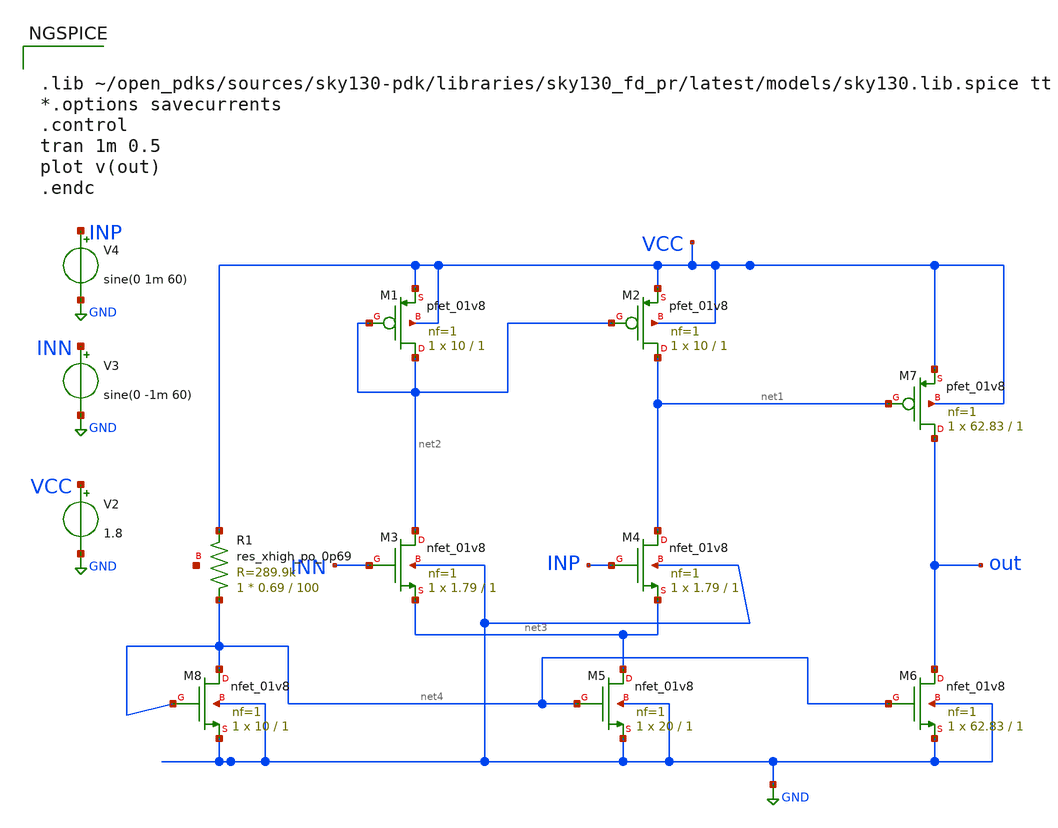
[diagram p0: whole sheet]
** sch_path: Week 4/xschem_180/comp_180.sch
**.subckt comp_180
XM1 net2 net2 VCC VCC sky130_fd_pr__pfet_01v8 L=1 W=10 nf=1 ad='int((nf+1)/2) * W/nf * 0.29' as='int((nf+2)/2) * W/nf * 0.29'
+ pd='2*int((nf+1)/2) * (W/nf + 0.29)' ps='2*int((nf+2)/2) * (W/nf + 0.29)' nrd='0.29 / W' nrs='0.29 / W'
+ sa=0 sb=0 sd=0 mult=1 m=1
XM2 net1 net2 VCC VCC sky130_fd_pr__pfet_01v8 L=1 W=10 nf=1 ad='int((nf+1)/2) * W/nf * 0.29' as='int((nf+2)/2) * W/nf * 0.29'
+ pd='2*int((nf+1)/2) * (W/nf + 0.29)' ps='2*int((nf+2)/2) * (W/nf + 0.29)' nrd='0.29 / W' nrs='0.29 / W'
+ sa=0 sb=0 sd=0 mult=1 m=1
XM3 net2 INN net3 GND sky130_fd_pr__nfet_01v8 L=1 W=1.79 nf=1 ad='int((nf+1)/2) * W/nf * 0.29' as='int((nf+2)/2) * W/nf * 0.29'
+ pd='2*int((nf+1)/2) * (W/nf + 0.29)' ps='2*int((nf+2)/2) * (W/nf + 0.29)' nrd='0.29 / W' nrs='0.29 / W'
+ sa=0 sb=0 sd=0 mult=1 m=1
XM4 net1 INP net3 GND sky130_fd_pr__nfet_01v8 L=1 W=1.79 nf=1 ad='int((nf+1)/2) * W/nf * 0.29' as='int((nf+2)/2) * W/nf * 0.29'
+ pd='2*int((nf+1)/2) * (W/nf + 0.29)' ps='2*int((nf+2)/2) * (W/nf + 0.29)' nrd='0.29 / W' nrs='0.29 / W'
+ sa=0 sb=0 sd=0 mult=1 m=1
XM5 net3 net4 GND GND sky130_fd_pr__nfet_01v8 L=1 W=20 nf=1 ad='int((nf+1)/2) * W/nf * 0.29' as='int((nf+2)/2) * W/nf * 0.29'
+ pd='2*int((nf+1)/2) * (W/nf + 0.29)' ps='2*int((nf+2)/2) * (W/nf + 0.29)' nrd='0.29 / W' nrs='0.29 / W'
+ sa=0 sb=0 sd=0 mult=1 m=1
XM6 out net4 GND GND sky130_fd_pr__nfet_01v8 L=1 W=62.83 nf=1 ad='int((nf+1)/2) * W/nf * 0.29' as='int((nf+2)/2) * W/nf * 0.29'
+ pd='2*int((nf+1)/2) * (W/nf + 0.29)' ps='2*int((nf+2)/2) * (W/nf + 0.29)' nrd='0.29 / W' nrs='0.29 / W'
+ sa=0 sb=0 sd=0 mult=1 m=1
XM7 out net1 VCC VCC sky130_fd_pr__pfet_01v8 L=1 W=62.83 nf=1 ad='int((nf+1)/2) * W/nf * 0.29' as='int((nf+2)/2) * W/nf * 0.29'
+ pd='2*int((nf+1)/2) * (W/nf + 0.29)' ps='2*int((nf+2)/2) * (W/nf + 0.29)' nrd='0.29 / W' nrs='0.29 / W'
+ sa=0 sb=0 sd=0 mult=1 m=1
V2 VCC GND 1.8
V3 INN GND sine(0 -1m 60)
V4 INP GND sine(0 1m 60)
XM8 net4 net4 GND GND sky130_fd_pr__nfet_01v8 L=1 W=10 nf=1 ad='int((nf+1)/2) * W/nf * 0.29' as='int((nf+2)/2) * W/nf * 0.29'
+ pd='2*int((nf+1)/2) * (W/nf + 0.29)' ps='2*int((nf+2)/2) * (W/nf + 0.29)' nrd='0.29 / W' nrs='0.29 / W'
+ sa=0 sb=0 sd=0 mult=1 m=1
XR1 net4 VCC net5 sky130_fd_pr__res_xhigh_po_0p69 L=100 mult=1 m=1
**** begin user architecture code


.lib ~/open_pdks/sources/sky130-pdk/libraries/sky130_fd_pr/latest/models/sky130.lib.spice tt
*.options savecurrents
.control
tran 1m 0.5
plot v(out)
.endc


**** end user architecture code
**.ends
.GLOBAL GND
.end
